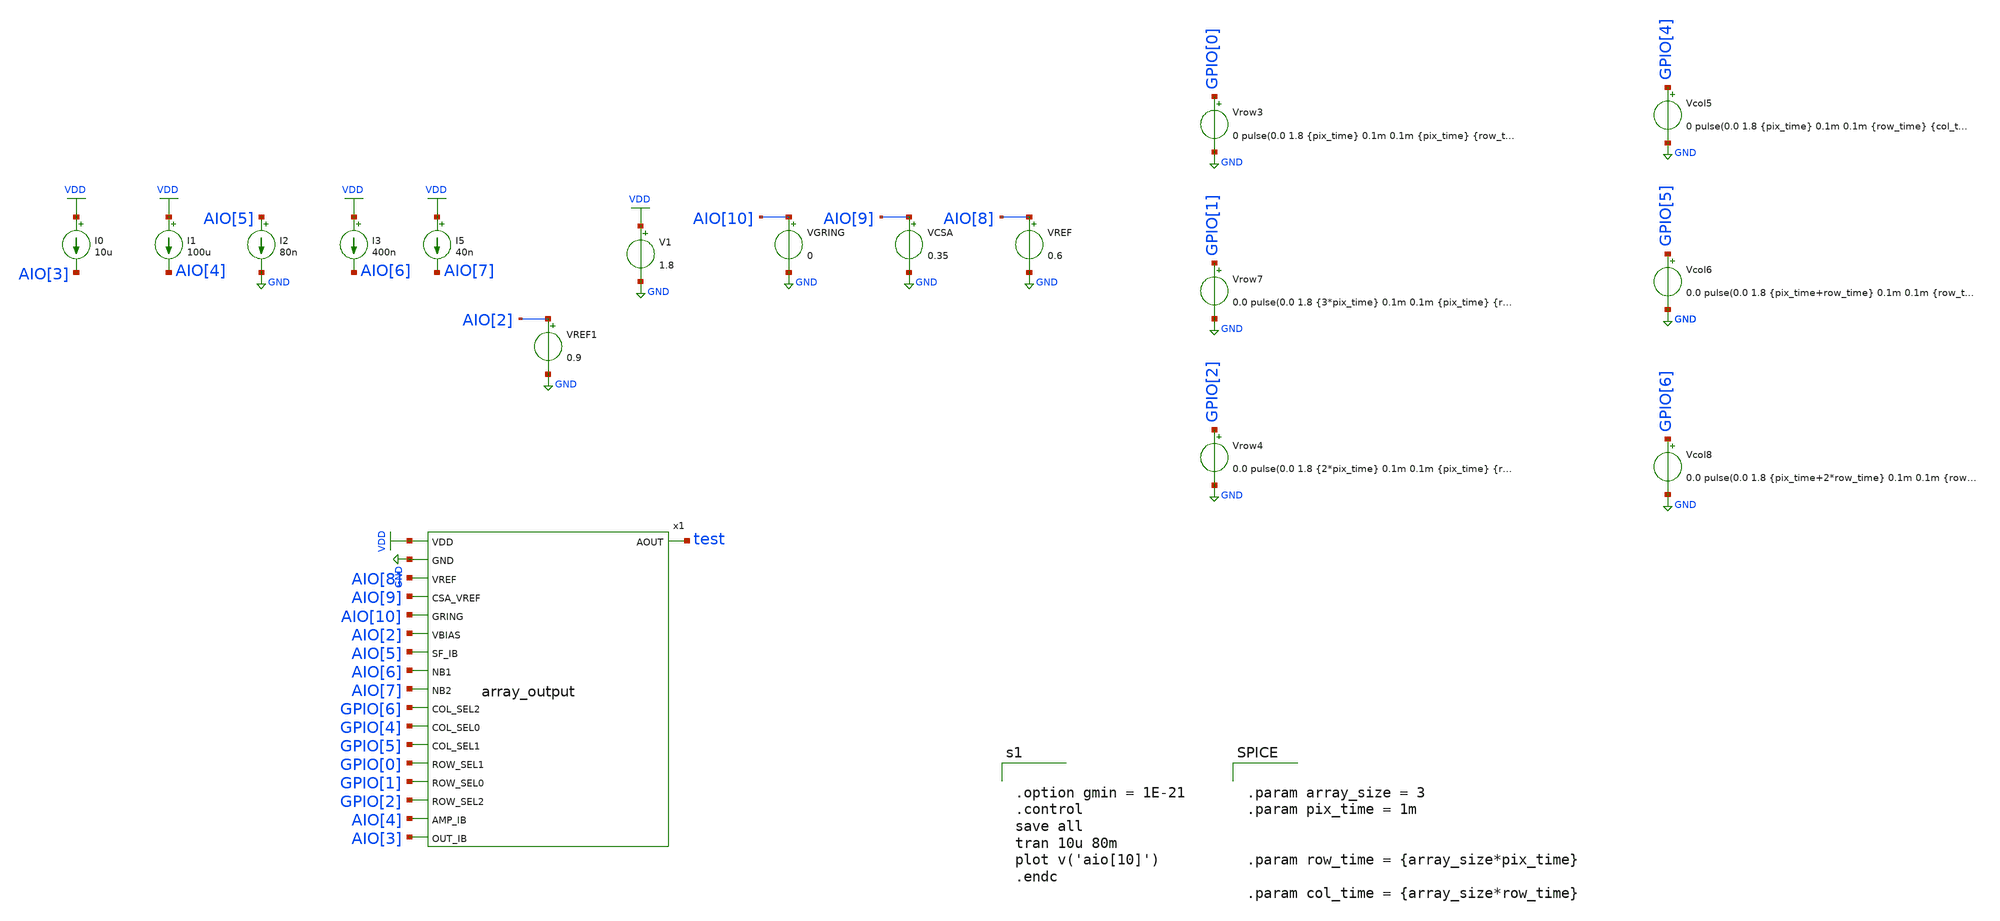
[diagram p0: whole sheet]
** sch_path: xschem/output_tb.sch
**.subckt output_tb
x1 VDD GND AIO[8] AIO[9] AIO[10] AIO[2] AIO[5] test AIO[6] AIO[7] GPIO[6] GPIO[4] GPIO[5] GPIO[0]
+ GPIO[1] GPIO[2] AIO[4] AIO[3] array_output
V1 VDD GND 1.8
VGRING AIO[10] GND 0
VCSA AIO[9] GND 0.35
VREF AIO[8] GND 0.6
Vrow3 GPIO[0] GND 0 pulse(0.0 1.8 {pix_time} 0.1m 0.1m {pix_time} {row_time})
Vrow4 GPIO[2] GND 0.0 pulse(0.0 1.8 {2*pix_time} 0.1m 0.1m {pix_time} {row_time})
Vcol5 GPIO[4] GND 0 pulse(0.0 1.8 {pix_time} 0.1m 0.1m {row_time} {col_time})
Vcol6 GPIO[5] GND 0.0 pulse(0.0 1.8 {pix_time+row_time} 0.1m 0.1m {row_time} {col_time})
Vrow7 GPIO[1] GND 0.0 pulse(0.0 1.8 {3*pix_time} 0.1m 0.1m {pix_time} {row_time})
Vcol8 GPIO[6] GND 0.0 pulse(0.0 1.8 {pix_time+2*row_time} 0.1m 0.1m {row_time} {col_time})
I0 VDD AIO[3] 10u
I1 VDD AIO[4] 100u
I2 AIO[5] GND 80n
I3 VDD AIO[6] 400n
I5 VDD AIO[7] 40n
VREF1 AIO[2] GND 0.9
**** begin user architecture code


.option gmin = 1E-21
.control
save all
tran 10u 80m
plot v('aio[10]')
.endc


** opencircuitdesign pdks install
.lib $::SKYWATER_MODELS/sky130.lib.spice tt




.param array_size = 3
.param pix_time = 1m


.param row_time = {array_size*pix_time}

.param col_time = {array_size*row_time}




**** end user architecture code
**.ends
.GLOBAL GND
.GLOBAL VDD
.end
